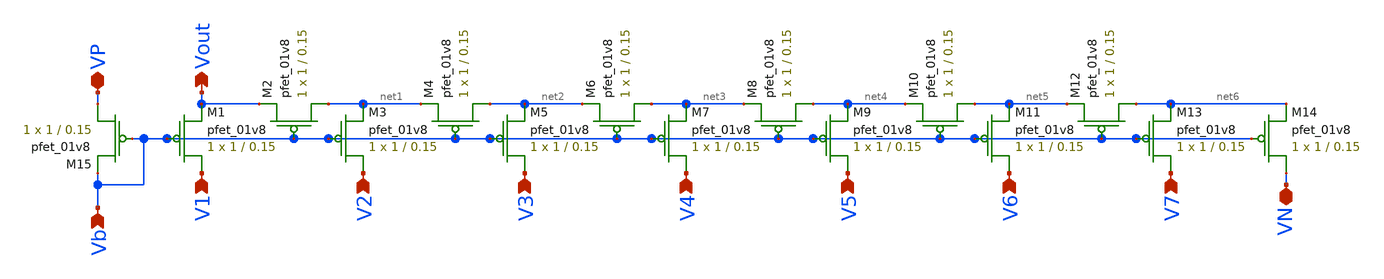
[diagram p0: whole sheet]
** sch_path: dac.sch
**.subckt dac VN VP V1 V2 V3 V4 V5 V6 V7 Vb Vout
*.iopin VN
*.iopin VP
*.ipin V1
*.ipin V2
*.ipin V3
*.ipin V4
*.ipin V5
*.ipin V6
*.ipin V7
*.ipin Vb
*.opin Vout
XM1 V1 Vb Vout VDD sky130_fd_pr__pfet_01v8 L=0.15 W=1 nf=1 ad='int((nf+1)/2) * W/nf * 0.29' as='int((nf+2)/2) * W/nf * 0.29'
+ pd='2*int((nf+1)/2) * (W/nf + 0.29)' ps='2*int((nf+2)/2) * (W/nf + 0.29)' nrd='0.29 / W' nrs='0.29 / W'
+ sa=0 sb=0 sd=0 mult=1 m=1
XM2 net1 Vb Vout VDD sky130_fd_pr__pfet_01v8 L=0.15 W=1 nf=1 ad='int((nf+1)/2) * W/nf * 0.29' as='int((nf+2)/2) * W/nf * 0.29'
+ pd='2*int((nf+1)/2) * (W/nf + 0.29)' ps='2*int((nf+2)/2) * (W/nf + 0.29)' nrd='0.29 / W' nrs='0.29 / W'
+ sa=0 sb=0 sd=0 mult=1 m=1
XM3 V2 Vb net1 VDD sky130_fd_pr__pfet_01v8 L=0.15 W=1 nf=1 ad='int((nf+1)/2) * W/nf * 0.29' as='int((nf+2)/2) * W/nf * 0.29'
+ pd='2*int((nf+1)/2) * (W/nf + 0.29)' ps='2*int((nf+2)/2) * (W/nf + 0.29)' nrd='0.29 / W' nrs='0.29 / W'
+ sa=0 sb=0 sd=0 mult=1 m=1
XM4 net2 Vb net1 VDD sky130_fd_pr__pfet_01v8 L=0.15 W=1 nf=1 ad='int((nf+1)/2) * W/nf * 0.29' as='int((nf+2)/2) * W/nf * 0.29'
+ pd='2*int((nf+1)/2) * (W/nf + 0.29)' ps='2*int((nf+2)/2) * (W/nf + 0.29)' nrd='0.29 / W' nrs='0.29 / W'
+ sa=0 sb=0 sd=0 mult=1 m=1
XM5 V3 Vb net2 VDD sky130_fd_pr__pfet_01v8 L=0.15 W=1 nf=1 ad='int((nf+1)/2) * W/nf * 0.29' as='int((nf+2)/2) * W/nf * 0.29'
+ pd='2*int((nf+1)/2) * (W/nf + 0.29)' ps='2*int((nf+2)/2) * (W/nf + 0.29)' nrd='0.29 / W' nrs='0.29 / W'
+ sa=0 sb=0 sd=0 mult=1 m=1
XM6 net3 Vb net2 VDD sky130_fd_pr__pfet_01v8 L=0.15 W=1 nf=1 ad='int((nf+1)/2) * W/nf * 0.29' as='int((nf+2)/2) * W/nf * 0.29'
+ pd='2*int((nf+1)/2) * (W/nf + 0.29)' ps='2*int((nf+2)/2) * (W/nf + 0.29)' nrd='0.29 / W' nrs='0.29 / W'
+ sa=0 sb=0 sd=0 mult=1 m=1
XM7 V4 Vb net3 VDD sky130_fd_pr__pfet_01v8 L=0.15 W=1 nf=1 ad='int((nf+1)/2) * W/nf * 0.29' as='int((nf+2)/2) * W/nf * 0.29'
+ pd='2*int((nf+1)/2) * (W/nf + 0.29)' ps='2*int((nf+2)/2) * (W/nf + 0.29)' nrd='0.29 / W' nrs='0.29 / W'
+ sa=0 sb=0 sd=0 mult=1 m=1
XM8 net4 Vb net3 VDD sky130_fd_pr__pfet_01v8 L=0.15 W=1 nf=1 ad='int((nf+1)/2) * W/nf * 0.29' as='int((nf+2)/2) * W/nf * 0.29'
+ pd='2*int((nf+1)/2) * (W/nf + 0.29)' ps='2*int((nf+2)/2) * (W/nf + 0.29)' nrd='0.29 / W' nrs='0.29 / W'
+ sa=0 sb=0 sd=0 mult=1 m=1
XM9 V5 Vb net4 VDD sky130_fd_pr__pfet_01v8 L=0.15 W=1 nf=1 ad='int((nf+1)/2) * W/nf * 0.29' as='int((nf+2)/2) * W/nf * 0.29'
+ pd='2*int((nf+1)/2) * (W/nf + 0.29)' ps='2*int((nf+2)/2) * (W/nf + 0.29)' nrd='0.29 / W' nrs='0.29 / W'
+ sa=0 sb=0 sd=0 mult=1 m=1
XM10 net5 Vb net4 VDD sky130_fd_pr__pfet_01v8 L=0.15 W=1 nf=1 ad='int((nf+1)/2) * W/nf * 0.29' as='int((nf+2)/2) * W/nf * 0.29'
+ pd='2*int((nf+1)/2) * (W/nf + 0.29)' ps='2*int((nf+2)/2) * (W/nf + 0.29)' nrd='0.29 / W' nrs='0.29 / W'
+ sa=0 sb=0 sd=0 mult=1 m=1
XM11 V6 Vb net5 VDD sky130_fd_pr__pfet_01v8 L=0.15 W=1 nf=1 ad='int((nf+1)/2) * W/nf * 0.29' as='int((nf+2)/2) * W/nf * 0.29'
+ pd='2*int((nf+1)/2) * (W/nf + 0.29)' ps='2*int((nf+2)/2) * (W/nf + 0.29)' nrd='0.29 / W' nrs='0.29 / W'
+ sa=0 sb=0 sd=0 mult=1 m=1
XM12 net6 Vb net5 VDD sky130_fd_pr__pfet_01v8 L=0.15 W=1 nf=1 ad='int((nf+1)/2) * W/nf * 0.29' as='int((nf+2)/2) * W/nf * 0.29'
+ pd='2*int((nf+1)/2) * (W/nf + 0.29)' ps='2*int((nf+2)/2) * (W/nf + 0.29)' nrd='0.29 / W' nrs='0.29 / W'
+ sa=0 sb=0 sd=0 mult=1 m=1
XM13 V7 Vb net6 VDD sky130_fd_pr__pfet_01v8 L=0.15 W=1 nf=1 ad='int((nf+1)/2) * W/nf * 0.29' as='int((nf+2)/2) * W/nf * 0.29'
+ pd='2*int((nf+1)/2) * (W/nf + 0.29)' ps='2*int((nf+2)/2) * (W/nf + 0.29)' nrd='0.29 / W' nrs='0.29 / W'
+ sa=0 sb=0 sd=0 mult=1 m=1
XM14 VN Vb net6 VDD sky130_fd_pr__pfet_01v8 L=0.15 W=1 nf=1 ad='int((nf+1)/2) * W/nf * 0.29' as='int((nf+2)/2) * W/nf * 0.29'
+ pd='2*int((nf+1)/2) * (W/nf + 0.29)' ps='2*int((nf+2)/2) * (W/nf + 0.29)' nrd='0.29 / W' nrs='0.29 / W'
+ sa=0 sb=0 sd=0 mult=1 m=1
XM15 VP Vb Vb VDD sky130_fd_pr__pfet_01v8 L=0.15 W=1 nf=1 ad='int((nf+1)/2) * W/nf * 0.29' as='int((nf+2)/2) * W/nf * 0.29'
+ pd='2*int((nf+1)/2) * (W/nf + 0.29)' ps='2*int((nf+2)/2) * (W/nf + 0.29)' nrd='0.29 / W' nrs='0.29 / W'
+ sa=0 sb=0 sd=0 mult=1 m=1
**.ends
.end
